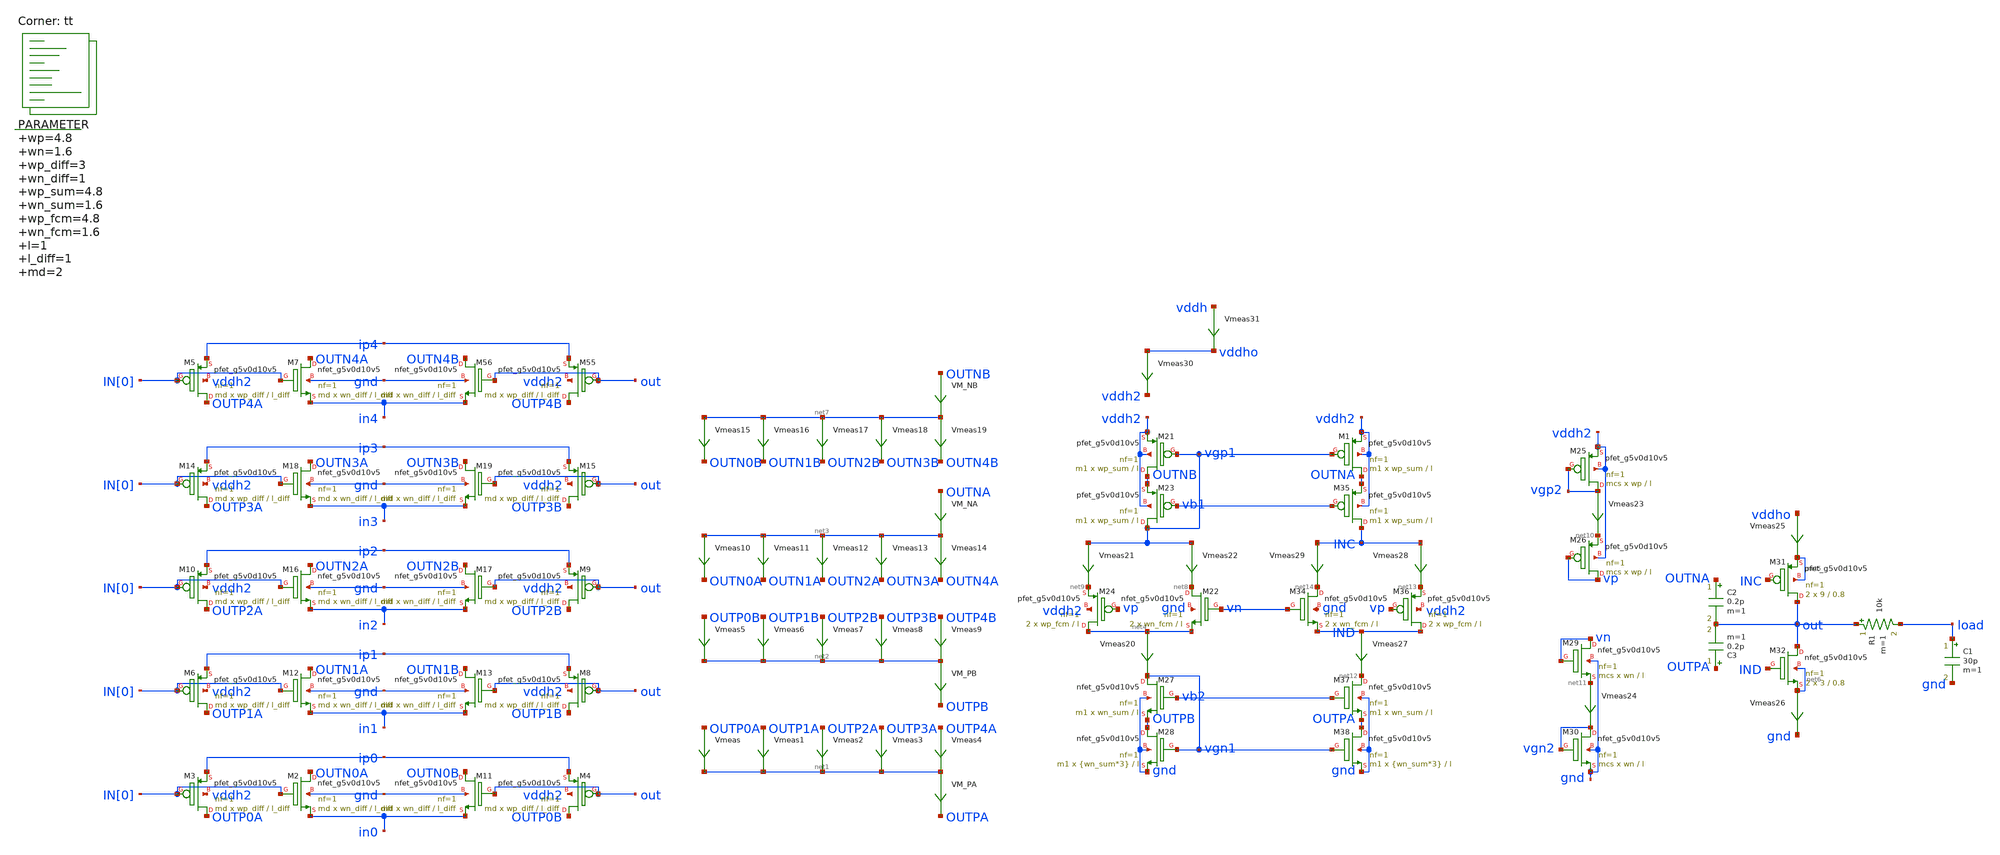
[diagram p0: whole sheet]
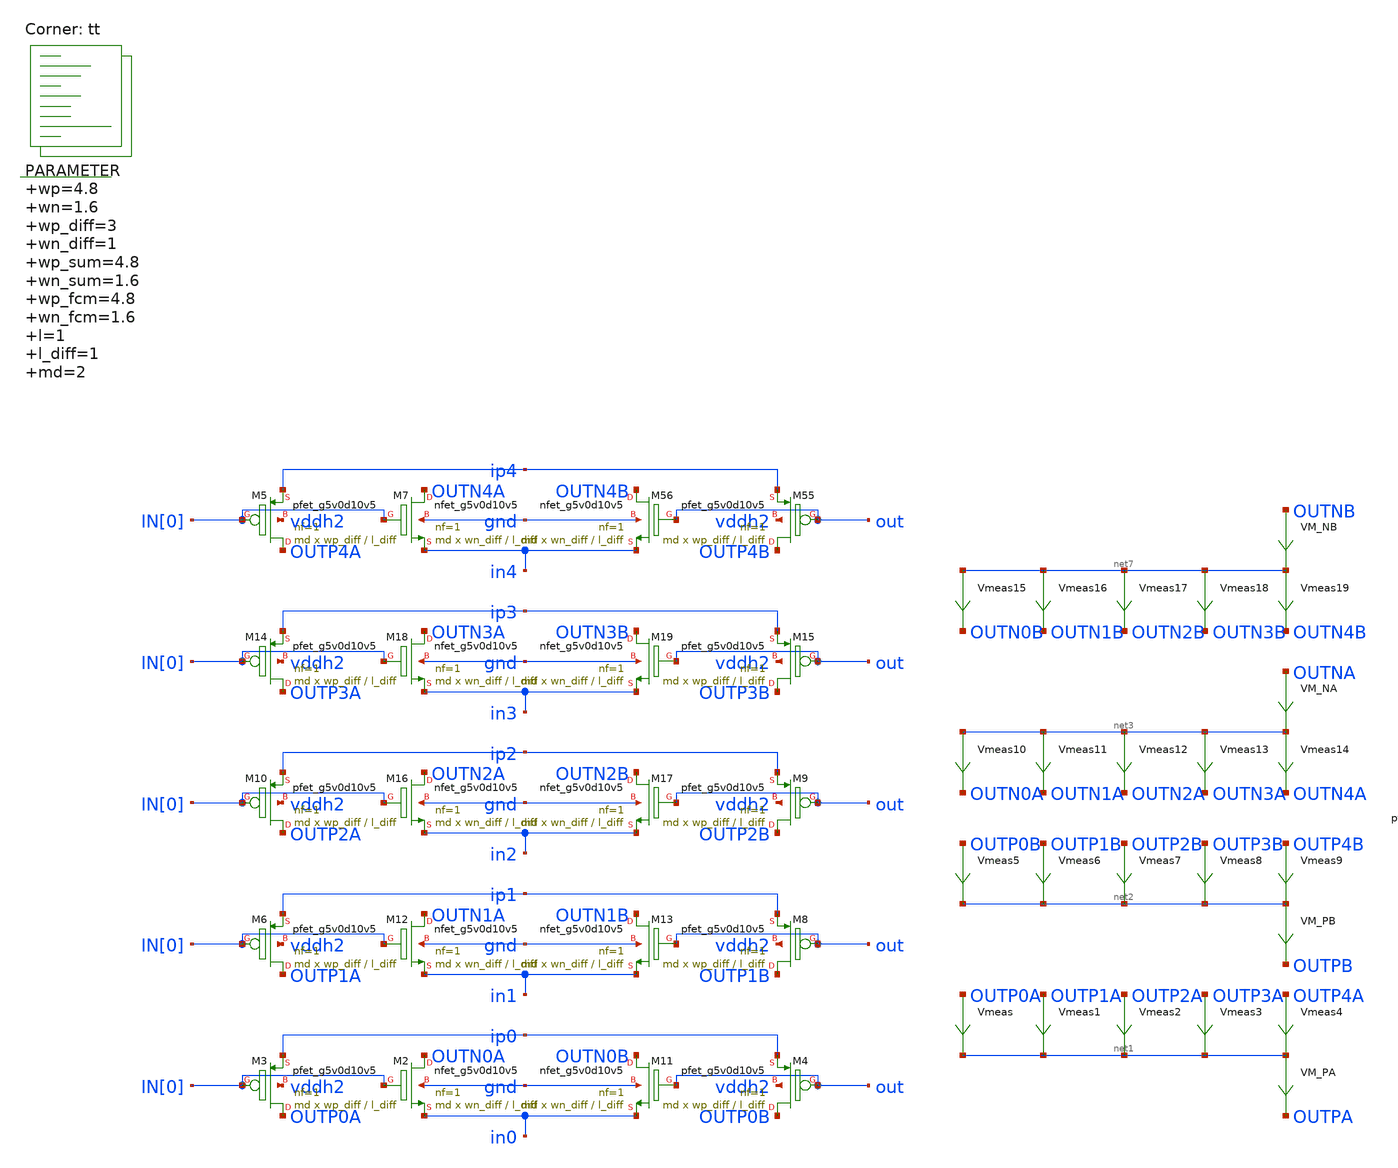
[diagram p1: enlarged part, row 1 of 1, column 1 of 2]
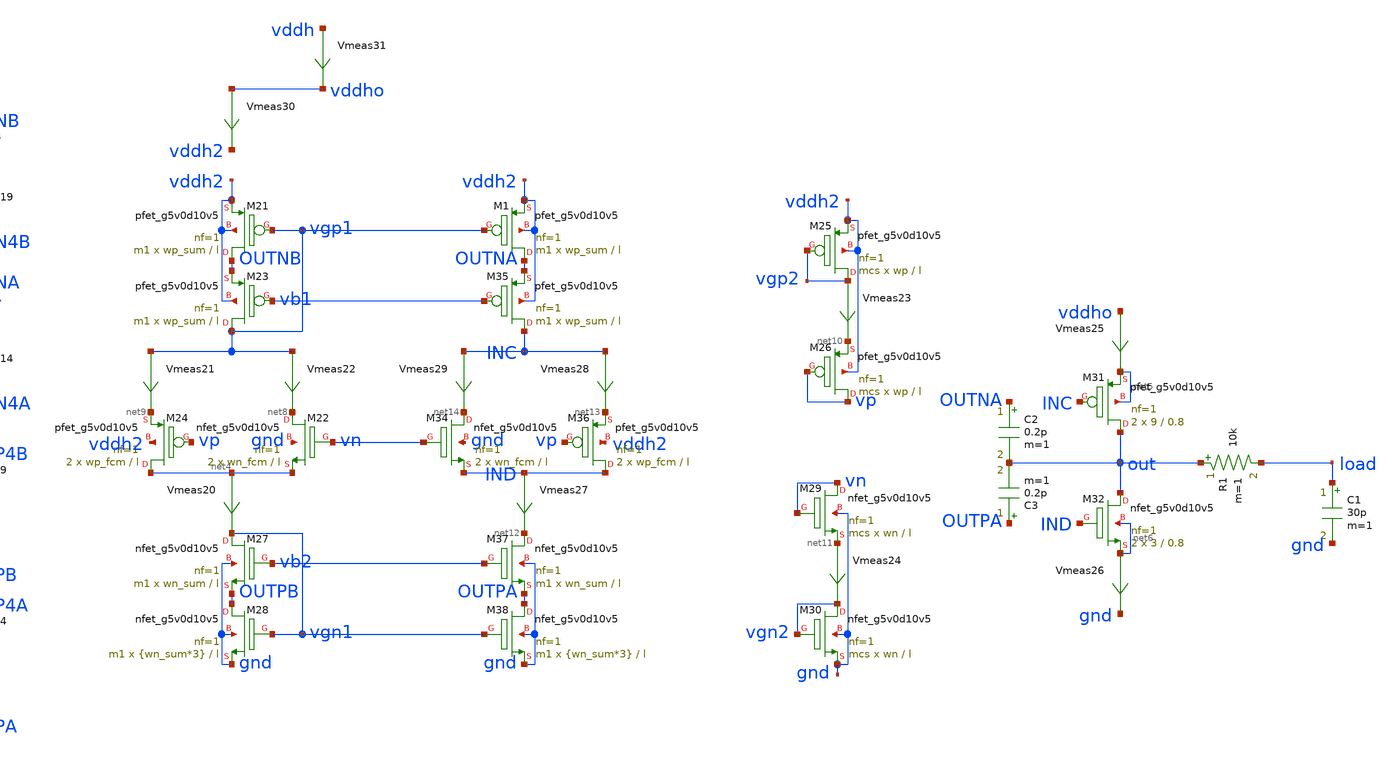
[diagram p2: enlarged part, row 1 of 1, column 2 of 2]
** sch_path: xschem/op_amp-tb.sch
**.subckt op_amp-tb
Vmeas OUTP0A net1 0
.save i(vmeas)
Vmeas1 OUTP1A net1 0
.save i(vmeas1)
Vmeas2 OUTP2A net1 0
.save i(vmeas2)
Vmeas3 OUTP3A net1 0
.save i(vmeas3)
Vmeas4 OUTP4A net1 0
.save i(vmeas4)
Vmeas5 OUTP0B net2 0
.save i(vmeas5)
Vmeas6 OUTP1B net2 0
.save i(vmeas6)
Vmeas7 OUTP2B net2 0
.save i(vmeas7)
Vmeas8 OUTP3B net2 0
.save i(vmeas8)
Vmeas9 OUTP4B net2 0
.save i(vmeas9)
Vmeas10 net3 OUTN0A 0
.save i(vmeas10)
Vmeas11 net3 OUTN1A 0
.save i(vmeas11)
Vmeas12 net3 OUTN2A 0
.save i(vmeas12)
Vmeas13 net3 OUTN3A 0
.save i(vmeas13)
Vmeas14 net3 OUTN4A 0
.save i(vmeas14)
Vmeas15 net7 OUTN0B 0
.save i(vmeas15)
Vmeas16 net7 OUTN1B 0
.save i(vmeas16)
Vmeas17 net7 OUTN2B 0
.save i(vmeas17)
Vmeas18 net7 OUTN3B 0
.save i(vmeas18)
Vmeas19 net7 OUTN4B 0
.save i(vmeas19)
.param wp=4.8 wn=1.6 wp_diff=3 wn_diff=1 wp_sum=4.8 wn_sum=1.6 wp_fcm=4.8 wn_fcm=1.6 l=1 l_diff=1
+ md=2 m1=2 mcs=2
Vmeas20 net4 vgn1 0
.save i(vmeas20)
XM22 net8 vn net4 gnd sky130_fd_pr__nfet_g5v0d10v5 L=l W=wn_fcm nf=1 ad='int((nf+1)/2) * W/nf * 0.29'
+ as='int((nf+2)/2) * W/nf * 0.29' pd='2*int((nf+1)/2) * (W/nf + 0.29)' ps='2*int((nf+2)/2) * (W/nf + 0.29)'
+ nrd='0.29 / W' nrs='0.29 / W' sa=0 sb=0 sd=0 mult=2 m=2
Vmeas21 vgp1 net9 0
.save i(vmeas21)
Vmeas22 vgp1 net8 0
.save i(vmeas22)
Vmeas23 vgp2 net10 0
.save i(vmeas23)
Vmeas24 net11 vgn2 0
.save i(vmeas24)
XM24 net4 vp net9 vddh2 sky130_fd_pr__pfet_g5v0d10v5 L=l W=wp_fcm nf=1 ad='int((nf+1)/2) * W/nf * 0.29'
+ as='int((nf+2)/2) * W/nf * 0.29' pd='2*int((nf+1)/2) * (W/nf + 0.29)' ps='2*int((nf+2)/2) * (W/nf + 0.29)'
+ nrd='0.29 / W' nrs='0.29 / W' sa=0 sb=0 sd=0 mult=2 m=2
XM25 vgp2 vgp2 vddh2 vddh2 sky130_fd_pr__pfet_g5v0d10v5 L=l W=wp nf=1 ad='int((nf+1)/2) * W/nf * 0.29'
+ as='int((nf+2)/2) * W/nf * 0.29' pd='2*int((nf+1)/2) * (W/nf + 0.29)' ps='2*int((nf+2)/2) * (W/nf + 0.29)'
+ nrd='0.29 / W' nrs='0.29 / W' sa=0 sb=0 sd=0 mult=mcs m=mcs
XM27 vgn1 vb2 OUTPB gnd sky130_fd_pr__nfet_g5v0d10v5 L=l W=wn_sum nf=1 ad='int((nf+1)/2) * W/nf * 0.29'
+ as='int((nf+2)/2) * W/nf * 0.29' pd='2*int((nf+1)/2) * (W/nf + 0.29)' ps='2*int((nf+2)/2) * (W/nf + 0.29)'
+ nrd='0.29 / W' nrs='0.29 / W' sa=0 sb=0 sd=0 mult=m1 m=m1
XM29 vn vn net11 gnd sky130_fd_pr__nfet_g5v0d10v5 L=l W=wn nf=1 ad='int((nf+1)/2) * W/nf * 0.29' as='int((nf+2)/2) * W/nf * 0.29'
+ pd='2*int((nf+1)/2) * (W/nf + 0.29)' ps='2*int((nf+2)/2) * (W/nf + 0.29)' nrd='0.29 / W' nrs='0.29 / W'
+ sa=0 sb=0 sd=0 mult=mcs m=mcs
XM31 out INC net5 net5 sky130_fd_pr__pfet_g5v0d10v5 L=0.8 W=9 nf=1 ad='int((nf+1)/2) * W/nf * 0.29' as='int((nf+2)/2) * W/nf * 0.29'
+ pd='2*int((nf+1)/2) * (W/nf + 0.29)' ps='2*int((nf+2)/2) * (W/nf + 0.29)' nrd='0.29 / W' nrs='0.29 / W'
+ sa=0 sb=0 sd=0 mult=2 m=2
XM32 out IND net6 net6 sky130_fd_pr__nfet_g5v0d10v5 L=0.8 W=3 nf=1 ad='int((nf+1)/2) * W/nf * 0.29' as='int((nf+2)/2) * W/nf * 0.29'
+ pd='2*int((nf+1)/2) * (W/nf + 0.29)' ps='2*int((nf+2)/2) * (W/nf + 0.29)' nrd='0.29 / W' nrs='0.29 / W'
+ sa=0 sb=0 sd=0 mult=2 m=2
Vmeas25 vddho net5 0
.save i(vmeas25)
Vmeas26 net6 gnd 0
.save i(vmeas26)
C1 load gnd 30p m=1
Vmeas27 IND net12 0
.save i(vmeas27)
Vmeas28 INC net13 0
.save i(vmeas28)
Vmeas29 INC net14 0
.save i(vmeas29)
VM_NB OUTNB net7 0
.save i(vm_nb)
VM_NA OUTNA net3 0
.save i(vm_na)
VM_PB net2 OUTPB 0
.save i(vm_pb)
VM_PA net1 OUTPA 0
.save i(vm_pa)
C2 OUTNA out 0.2p m=1
C3 OUTPA out 0.2p m=1
XM21 OUTNB vgp1 vddh2 vddh2 sky130_fd_pr__pfet_g5v0d10v5 L=l W=wp_sum nf=1 ad='int((nf+1)/2) * W/nf * 0.29'
+ as='int((nf+2)/2) * W/nf * 0.29' pd='2*int((nf+1)/2) * (W/nf + 0.29)' ps='2*int((nf+2)/2) * (W/nf + 0.29)'
+ nrd='0.29 / W' nrs='0.29 / W' sa=0 sb=0 sd=0 mult=m1 m=m1
XM23 vgp1 vb1 OUTNB vddh2 sky130_fd_pr__pfet_g5v0d10v5 L=l W=wp_sum nf=1 ad='int((nf+1)/2) * W/nf * 0.29'
+ as='int((nf+2)/2) * W/nf * 0.29' pd='2*int((nf+1)/2) * (W/nf + 0.29)' ps='2*int((nf+2)/2) * (W/nf + 0.29)'
+ nrd='0.29 / W' nrs='0.29 / W' sa=0 sb=0 sd=0 mult=m1 m=m1
XM35 INC vb1 OUTNA vddh2 sky130_fd_pr__pfet_g5v0d10v5 L=l W=wp_sum nf=1 ad='int((nf+1)/2) * W/nf * 0.29'
+ as='int((nf+2)/2) * W/nf * 0.29' pd='2*int((nf+1)/2) * (W/nf + 0.29)' ps='2*int((nf+2)/2) * (W/nf + 0.29)'
+ nrd='0.29 / W' nrs='0.29 / W' sa=0 sb=0 sd=0 mult=m1 m=m1
XM28 OUTPB vgn1 gnd gnd sky130_fd_pr__nfet_g5v0d10v5 L=l W={wn_sum*3} nf=1 ad='int((nf+1)/2) * W/nf * 0.29'
+ as='int((nf+2)/2) * W/nf * 0.29' pd='2*int((nf+1)/2) * (W/nf + 0.29)' ps='2*int((nf+2)/2) * (W/nf + 0.29)'
+ nrd='0.29 / W' nrs='0.29 / W' sa=0 sb=0 sd=0 mult=m1 m=m1
XM37 net12 vb2 OUTPA gnd sky130_fd_pr__nfet_g5v0d10v5 L=l W=wn_sum nf=1 ad='int((nf+1)/2) * W/nf * 0.29'
+ as='int((nf+2)/2) * W/nf * 0.29' pd='2*int((nf+1)/2) * (W/nf + 0.29)' ps='2*int((nf+2)/2) * (W/nf + 0.29)'
+ nrd='0.29 / W' nrs='0.29 / W' sa=0 sb=0 sd=0 mult=m1 m=m1
Vmeas30 vddho vddh2 0
.save i(vmeas30)
Vmeas31 vddh vddho 0
.save i(vmeas31)
R1 out load 10k m=1
XM26 vp vp net10 vddh2 sky130_fd_pr__pfet_g5v0d10v5 L=l W=wp nf=1 ad='int((nf+1)/2) * W/nf * 0.29' as='int((nf+2)/2) * W/nf * 0.29'
+ pd='2*int((nf+1)/2) * (W/nf + 0.29)' ps='2*int((nf+2)/2) * (W/nf + 0.29)' nrd='0.29 / W' nrs='0.29 / W'
+ sa=0 sb=0 sd=0 mult=mcs m=mcs
XM30 vgn2 vgn2 gnd gnd sky130_fd_pr__nfet_g5v0d10v5 L=l W=wn nf=1 ad='int((nf+1)/2) * W/nf * 0.29' as='int((nf+2)/2) * W/nf * 0.29'
+ pd='2*int((nf+1)/2) * (W/nf + 0.29)' ps='2*int((nf+2)/2) * (W/nf + 0.29)' nrd='0.29 / W' nrs='0.29 / W'
+ sa=0 sb=0 sd=0 mult=mcs m=mcs
XM1 OUTNA vgp1 vddh2 vddh2 sky130_fd_pr__pfet_g5v0d10v5 L=l W=wp_sum nf=1 ad='int((nf+1)/2) * W/nf * 0.29'
+ as='int((nf+2)/2) * W/nf * 0.29' pd='2*int((nf+1)/2) * (W/nf + 0.29)' ps='2*int((nf+2)/2) * (W/nf + 0.29)'
+ nrd='0.29 / W' nrs='0.29 / W' sa=0 sb=0 sd=0 mult=m1 m=m1
XM2 OUTN0A IN[0] in0 gnd sky130_fd_pr__nfet_g5v0d10v5 L=l_diff W=wn_diff nf=1 ad='int((nf+1)/2) * W/nf * 0.29'
+ as='int((nf+2)/2) * W/nf * 0.29' pd='2*int((nf+1)/2) * (W/nf + 0.29)' ps='2*int((nf+2)/2) * (W/nf + 0.29)'
+ nrd='0.29 / W' nrs='0.29 / W' sa=0 sb=0 sd=0 mult=md m=md
XM3 OUTP0A IN[0] ip0 vddh2 sky130_fd_pr__pfet_g5v0d10v5 L=l_diff W=wp_diff nf=1 ad='int((nf+1)/2) * W/nf * 0.29'
+ as='int((nf+2)/2) * W/nf * 0.29' pd='2*int((nf+1)/2) * (W/nf + 0.29)' ps='2*int((nf+2)/2) * (W/nf + 0.29)'
+ nrd='0.29 / W' nrs='0.29 / W' sa=0 sb=0 sd=0 mult=md m=md
XM4 OUTP0B out ip0 vddh2 sky130_fd_pr__pfet_g5v0d10v5 L=l_diff W=wp_diff nf=1 ad='int((nf+1)/2) * W/nf * 0.29'
+ as='int((nf+2)/2) * W/nf * 0.29' pd='2*int((nf+1)/2) * (W/nf + 0.29)' ps='2*int((nf+2)/2) * (W/nf + 0.29)'
+ nrd='0.29 / W' nrs='0.29 / W' sa=0 sb=0 sd=0 mult=md m=md
XM6 OUTP1A IN[0] ip1 vddh2 sky130_fd_pr__pfet_g5v0d10v5 L=l_diff W=wp_diff nf=1 ad='int((nf+1)/2) * W/nf * 0.29'
+ as='int((nf+2)/2) * W/nf * 0.29' pd='2*int((nf+1)/2) * (W/nf + 0.29)' ps='2*int((nf+2)/2) * (W/nf + 0.29)'
+ nrd='0.29 / W' nrs='0.29 / W' sa=0 sb=0 sd=0 mult=md m=md
XM8 OUTP1B out ip1 vddh2 sky130_fd_pr__pfet_g5v0d10v5 L=l_diff W=wp_diff nf=1 ad='int((nf+1)/2) * W/nf * 0.29'
+ as='int((nf+2)/2) * W/nf * 0.29' pd='2*int((nf+1)/2) * (W/nf + 0.29)' ps='2*int((nf+2)/2) * (W/nf + 0.29)'
+ nrd='0.29 / W' nrs='0.29 / W' sa=0 sb=0 sd=0 mult=md m=md
XM11 OUTN0B out in0 gnd sky130_fd_pr__nfet_g5v0d10v5 L=l_diff W=wn_diff nf=1 ad='int((nf+1)/2) * W/nf * 0.29'
+ as='int((nf+2)/2) * W/nf * 0.29' pd='2*int((nf+1)/2) * (W/nf + 0.29)' ps='2*int((nf+2)/2) * (W/nf + 0.29)'
+ nrd='0.29 / W' nrs='0.29 / W' sa=0 sb=0 sd=0 mult=md m=md
XM12 OUTN1A IN[0] in1 gnd sky130_fd_pr__nfet_g5v0d10v5 L=l_diff W=wn_diff nf=1 ad='int((nf+1)/2) * W/nf * 0.29'
+ as='int((nf+2)/2) * W/nf * 0.29' pd='2*int((nf+1)/2) * (W/nf + 0.29)' ps='2*int((nf+2)/2) * (W/nf + 0.29)'
+ nrd='0.29 / W' nrs='0.29 / W' sa=0 sb=0 sd=0 mult=md m=md
XM13 OUTN1B out in1 gnd sky130_fd_pr__nfet_g5v0d10v5 L=l_diff W=wn_diff nf=1 ad='int((nf+1)/2) * W/nf * 0.29'
+ as='int((nf+2)/2) * W/nf * 0.29' pd='2*int((nf+1)/2) * (W/nf + 0.29)' ps='2*int((nf+2)/2) * (W/nf + 0.29)'
+ nrd='0.29 / W' nrs='0.29 / W' sa=0 sb=0 sd=0 mult=md m=md
XM36 IND vp net13 vddh2 sky130_fd_pr__pfet_g5v0d10v5 L=l W=wp_fcm nf=1 ad='int((nf+1)/2) * W/nf * 0.29'
+ as='int((nf+2)/2) * W/nf * 0.29' pd='2*int((nf+1)/2) * (W/nf + 0.29)' ps='2*int((nf+2)/2) * (W/nf + 0.29)'
+ nrd='0.29 / W' nrs='0.29 / W' sa=0 sb=0 sd=0 mult=2 m=2
XM34 net14 vn IND gnd sky130_fd_pr__nfet_g5v0d10v5 L=l W=wn_fcm nf=1 ad='int((nf+1)/2) * W/nf * 0.29'
+ as='int((nf+2)/2) * W/nf * 0.29' pd='2*int((nf+1)/2) * (W/nf + 0.29)' ps='2*int((nf+2)/2) * (W/nf + 0.29)'
+ nrd='0.29 / W' nrs='0.29 / W' sa=0 sb=0 sd=0 mult=2 m=2
XM38 OUTPA vgn1 gnd gnd sky130_fd_pr__nfet_g5v0d10v5 L=l W={wn_sum*3} nf=1 ad='int((nf+1)/2) * W/nf * 0.29'
+ as='int((nf+2)/2) * W/nf * 0.29' pd='2*int((nf+1)/2) * (W/nf + 0.29)' ps='2*int((nf+2)/2) * (W/nf + 0.29)'
+ nrd='0.29 / W' nrs='0.29 / W' sa=0 sb=0 sd=0 mult=m1 m=m1
XM5 OUTP4A IN[0] ip4 vddh2 sky130_fd_pr__pfet_g5v0d10v5 L=l_diff W=wp_diff nf=1 ad='int((nf+1)/2) * W/nf * 0.29'
+ as='int((nf+2)/2) * W/nf * 0.29' pd='2*int((nf+1)/2) * (W/nf + 0.29)' ps='2*int((nf+2)/2) * (W/nf + 0.29)'
+ nrd='0.29 / W' nrs='0.29 / W' sa=0 sb=0 sd=0 mult=md m=md
XM7 OUTN4A IN[0] in4 gnd sky130_fd_pr__nfet_g5v0d10v5 L=l_diff W=wn_diff nf=1 ad='int((nf+1)/2) * W/nf * 0.29'
+ as='int((nf+2)/2) * W/nf * 0.29' pd='2*int((nf+1)/2) * (W/nf + 0.29)' ps='2*int((nf+2)/2) * (W/nf + 0.29)'
+ nrd='0.29 / W' nrs='0.29 / W' sa=0 sb=0 sd=0 mult=md m=md
XM55 OUTP4B out ip4 vddh2 sky130_fd_pr__pfet_g5v0d10v5 L=l_diff W=wp_diff nf=1 ad='int((nf+1)/2) * W/nf * 0.29'
+ as='int((nf+2)/2) * W/nf * 0.29' pd='2*int((nf+1)/2) * (W/nf + 0.29)' ps='2*int((nf+2)/2) * (W/nf + 0.29)'
+ nrd='0.29 / W' nrs='0.29 / W' sa=0 sb=0 sd=0 mult=md m=md
XM56 OUTN4B out in4 gnd sky130_fd_pr__nfet_g5v0d10v5 L=l_diff W=wn_diff nf=1 ad='int((nf+1)/2) * W/nf * 0.29'
+ as='int((nf+2)/2) * W/nf * 0.29' pd='2*int((nf+1)/2) * (W/nf + 0.29)' ps='2*int((nf+2)/2) * (W/nf + 0.29)'
+ nrd='0.29 / W' nrs='0.29 / W' sa=0 sb=0 sd=0 mult=md m=md
XM10 OUTP2A IN[0] ip2 vddh2 sky130_fd_pr__pfet_g5v0d10v5 L=l_diff W=wp_diff nf=1 ad='int((nf+1)/2) * W/nf * 0.29'
+ as='int((nf+2)/2) * W/nf * 0.29' pd='2*int((nf+1)/2) * (W/nf + 0.29)' ps='2*int((nf+2)/2) * (W/nf + 0.29)'
+ nrd='0.29 / W' nrs='0.29 / W' sa=0 sb=0 sd=0 mult=md m=md
XM9 OUTP2B out ip2 vddh2 sky130_fd_pr__pfet_g5v0d10v5 L=l_diff W=wp_diff nf=1 ad='int((nf+1)/2) * W/nf * 0.29'
+ as='int((nf+2)/2) * W/nf * 0.29' pd='2*int((nf+1)/2) * (W/nf + 0.29)' ps='2*int((nf+2)/2) * (W/nf + 0.29)'
+ nrd='0.29 / W' nrs='0.29 / W' sa=0 sb=0 sd=0 mult=md m=md
XM14 OUTP3A IN[0] ip3 vddh2 sky130_fd_pr__pfet_g5v0d10v5 L=l_diff W=wp_diff nf=1 ad='int((nf+1)/2) * W/nf * 0.29'
+ as='int((nf+2)/2) * W/nf * 0.29' pd='2*int((nf+1)/2) * (W/nf + 0.29)' ps='2*int((nf+2)/2) * (W/nf + 0.29)'
+ nrd='0.29 / W' nrs='0.29 / W' sa=0 sb=0 sd=0 mult=md m=md
XM15 OUTP3B out ip3 vddh2 sky130_fd_pr__pfet_g5v0d10v5 L=l_diff W=wp_diff nf=1 ad='int((nf+1)/2) * W/nf * 0.29'
+ as='int((nf+2)/2) * W/nf * 0.29' pd='2*int((nf+1)/2) * (W/nf + 0.29)' ps='2*int((nf+2)/2) * (W/nf + 0.29)'
+ nrd='0.29 / W' nrs='0.29 / W' sa=0 sb=0 sd=0 mult=md m=md
XM16 OUTN2A IN[0] in2 gnd sky130_fd_pr__nfet_g5v0d10v5 L=l_diff W=wn_diff nf=1 ad='int((nf+1)/2) * W/nf * 0.29'
+ as='int((nf+2)/2) * W/nf * 0.29' pd='2*int((nf+1)/2) * (W/nf + 0.29)' ps='2*int((nf+2)/2) * (W/nf + 0.29)'
+ nrd='0.29 / W' nrs='0.29 / W' sa=0 sb=0 sd=0 mult=md m=md
XM17 OUTN2B out in2 gnd sky130_fd_pr__nfet_g5v0d10v5 L=l_diff W=wn_diff nf=1 ad='int((nf+1)/2) * W/nf * 0.29'
+ as='int((nf+2)/2) * W/nf * 0.29' pd='2*int((nf+1)/2) * (W/nf + 0.29)' ps='2*int((nf+2)/2) * (W/nf + 0.29)'
+ nrd='0.29 / W' nrs='0.29 / W' sa=0 sb=0 sd=0 mult=md m=md
XM18 OUTN3A IN[0] in3 gnd sky130_fd_pr__nfet_g5v0d10v5 L=l_diff W=wn_diff nf=1 ad='int((nf+1)/2) * W/nf * 0.29'
+ as='int((nf+2)/2) * W/nf * 0.29' pd='2*int((nf+1)/2) * (W/nf + 0.29)' ps='2*int((nf+2)/2) * (W/nf + 0.29)'
+ nrd='0.29 / W' nrs='0.29 / W' sa=0 sb=0 sd=0 mult=md m=md
XM19 OUTN3B out in3 gnd sky130_fd_pr__nfet_g5v0d10v5 L=l_diff W=wn_diff nf=1 ad='int((nf+1)/2) * W/nf * 0.29'
+ as='int((nf+2)/2) * W/nf * 0.29' pd='2*int((nf+1)/2) * (W/nf + 0.29)' ps='2*int((nf+2)/2) * (W/nf + 0.29)'
+ nrd='0.29 / W' nrs='0.29 / W' sa=0 sb=0 sd=0 mult=md m=md
**** begin user architecture code
.lib $::SKYWATER_MODELS/sky130.lib.spice tt



  .option wnflag=1
  .option safecurrents
  ********************Static Current Sources***************************
  .param base_current=40n
  .param i0=base_current i1={1*i0} i2={2*i0} i3={4*i0} i4={8*i0}
  Ip0 vddh ip0 i0
  In0 in0  gnd i0

  Ip1 vddh ip1 i1
  In1 in1  gnd i1

  Ip2 vddh ip2 i2
  In2 in2  gnd i2

  Ip3 vddh ip3 i3
  In3 in3  gnd i3

  Ip4 vddh ip4 i4
  In4 in4  gnd i4

  Ivp vp gnd 100n
  Ivn vddh vn 100n
  ********************Static Voltage Sources***************************
  Vddh vddh gnd dc 5.5

  vb1 vb1 gnd dc 3.2
  vb2 vb2 gnd dc 2
  ********************Dynamic Voltage Sources***************************
  *******Calculation**********
  .param base_f=100e3 base_t={1/base_f} base_th={base_t/2} base_d={base_th}
  .param b0_th={base_th} b0_t={b0_th*2}
  .param b1_th={b0_th*2} b1_t={b1_th*2}
  .param b2_th={b1_th*2} b2_t={b2_th*2}
  .param b3_th={b2_th*2} b3_t={b3_th*2}
  *******Signals**********
  .param vh=1.162 vl=1.044
  vin0 in[0] gnd dc pulse(5.5 0 {base_d} 1n 1n {b0_th} {b0_t})
  *vin0 in[0] gnd dc vl
  *Vin1 in[1] gnd pulse({vh} {vl} {base_d} 1n 1n {b0_th} {b0_t})
  *Vin2 in[2] gnd pulse({vh} {vl} {base_d} 1n 1n {b1_th} {b1_t})
  *Vin3 in[3] gnd pulse({vh} {vl} {base_d} 1n 1n {b2_th} {b2_t})
  *Vin4 in[4] gnd pulse({vh} {vl} {base_d} 1n 1n {b3_th} {b3_t})
  ********************Simulation Commands*****************************
  .control
     reset
     op
     write op_amp-tb.raw

     tran 1n 100u
     *dc vin0 -1 6.5 0.01
     *ac dec 100 1 1e9

     let vout_mag =abs(v(out))
     let vout_phase_margin = phase(v(out))*180/pi + 180
     meas ac Aol find vout_mag at = 10
     meas ac UGF when vout_mag=1 fall=1
     meas ac PM find vout_phase_margin when vout_mag=1
     let difference = v(inc) - v(ind)
     save difference
     write op_amp-tb.raw

     set wr_vecnames
     set wr_singlescale
     wrdata /home/yohanes/10-bit-DAC/simulations/op_amp222-tb.txt out load
*    quit 0
  .endc





*.save out load IN[0] IN[1] IN[2] IN[3] IN[4]
.save all


**** end user architecture code
**.ends
.end
